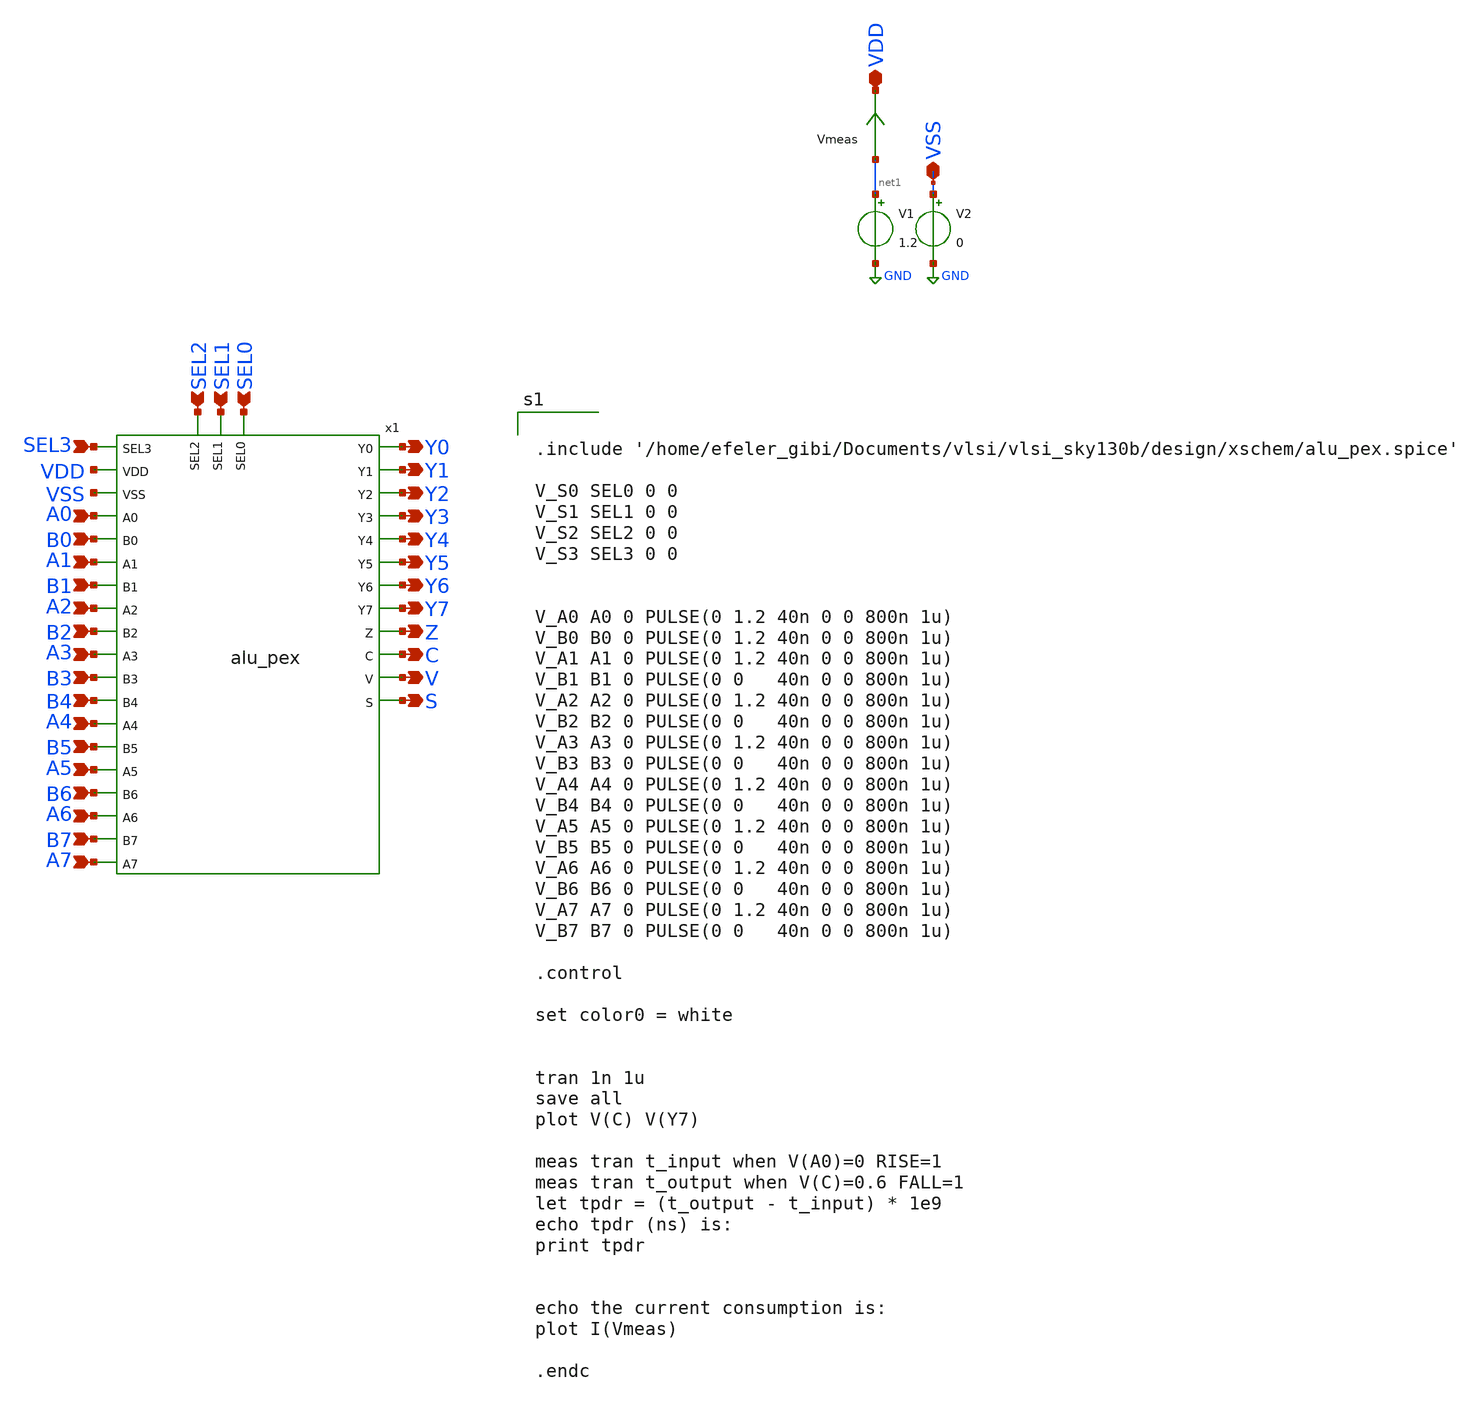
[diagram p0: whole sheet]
** sch_path: design/xschem/TEST_BENCHES/ALUpex_TB_delay.sch
**.subckt ALUpex_TB_delay VDD VSS A7 A6 A5 A4 A3 A2 A1 A0 B1 B2 B3 B0 B6 B7 B5 B4 Y0 Y1 Y2 Y3 Y4 Y5
*+ Y6 Y7 Z C V S SEL0 SEL1 SEL2 SEL3
*.iopin VDD
*.iopin VSS
*.ipin A7
*.ipin A6
*.ipin A5
*.ipin A4
*.ipin A3
*.ipin A2
*.ipin A1
*.ipin A0
*.ipin B1
*.ipin B2
*.ipin B3
*.ipin B0
*.ipin B6
*.ipin B7
*.ipin B5
*.ipin B4
*.opin Y0
*.opin Y1
*.opin Y2
*.opin Y3
*.opin Y4
*.opin Y5
*.opin Y6
*.opin Y7
*.opin Z
*.opin C
*.opin V
*.opin S
*.ipin SEL0
*.ipin SEL1
*.ipin SEL2
*.ipin SEL3
V1 net1 GND 1.2
V2 VSS GND 0
x1 SEL3 A0 B0 Y0 Z VDD VSS A1 C B1 Y1 A2 V B2 Y2 S A3 Y3 B3 B4 Y4 A4 B5 A5 Y5 B6 Y6 A6 B7 Y7 A7 SEL2
+ SEL1 SEL0 alu_pex
Vmeas net1 VDD 0
.save i(vmeas)
**** begin user architecture code

** opencircuitdesign pdks install
.lib $::SKYWATER_MODELS/sky130.lib.spice tt_mm




.include '/home/efeler_gibi/Documents/vlsi/vlsi_sky130b/design/xschem/alu_pex.spice'

V_S0 SEL0 0 0
V_S1 SEL1 0 0
V_S2 SEL2 0 0
V_S3 SEL3 0 0


V_A0 A0 0 PULSE(0 1.2 40n 0 0 800n 1u)
V_B0 B0 0 PULSE(0 1.2 40n 0 0 800n 1u)
V_A1 A1 0 PULSE(0 1.2 40n 0 0 800n 1u)
V_B1 B1 0 PULSE(0 0   40n 0 0 800n 1u)
V_A2 A2 0 PULSE(0 1.2 40n 0 0 800n 1u)
V_B2 B2 0 PULSE(0 0   40n 0 0 800n 1u)
V_A3 A3 0 PULSE(0 1.2 40n 0 0 800n 1u)
V_B3 B3 0 PULSE(0 0   40n 0 0 800n 1u)
V_A4 A4 0 PULSE(0 1.2 40n 0 0 800n 1u)
V_B4 B4 0 PULSE(0 0   40n 0 0 800n 1u)
V_A5 A5 0 PULSE(0 1.2 40n 0 0 800n 1u)
V_B5 B5 0 PULSE(0 0   40n 0 0 800n 1u)
V_A6 A6 0 PULSE(0 1.2 40n 0 0 800n 1u)
V_B6 B6 0 PULSE(0 0   40n 0 0 800n 1u)
V_A7 A7 0 PULSE(0 1.2 40n 0 0 800n 1u)
V_B7 B7 0 PULSE(0 0   40n 0 0 800n 1u)

.control

set color0 = white


tran 1n 1u
save all
plot V(C) V(Y7)

meas tran t_input when V(A0)=0 RISE=1
meas tran t_output when V(C)=0.6 FALL=1
let tpdr = (t_output - t_input) * 1e9
echo tpdr (ns) is:
print tpdr


echo the current consumption is:
plot I(Vmeas)

.endc



**** end user architecture code
**.ends
.GLOBAL GND
.end
